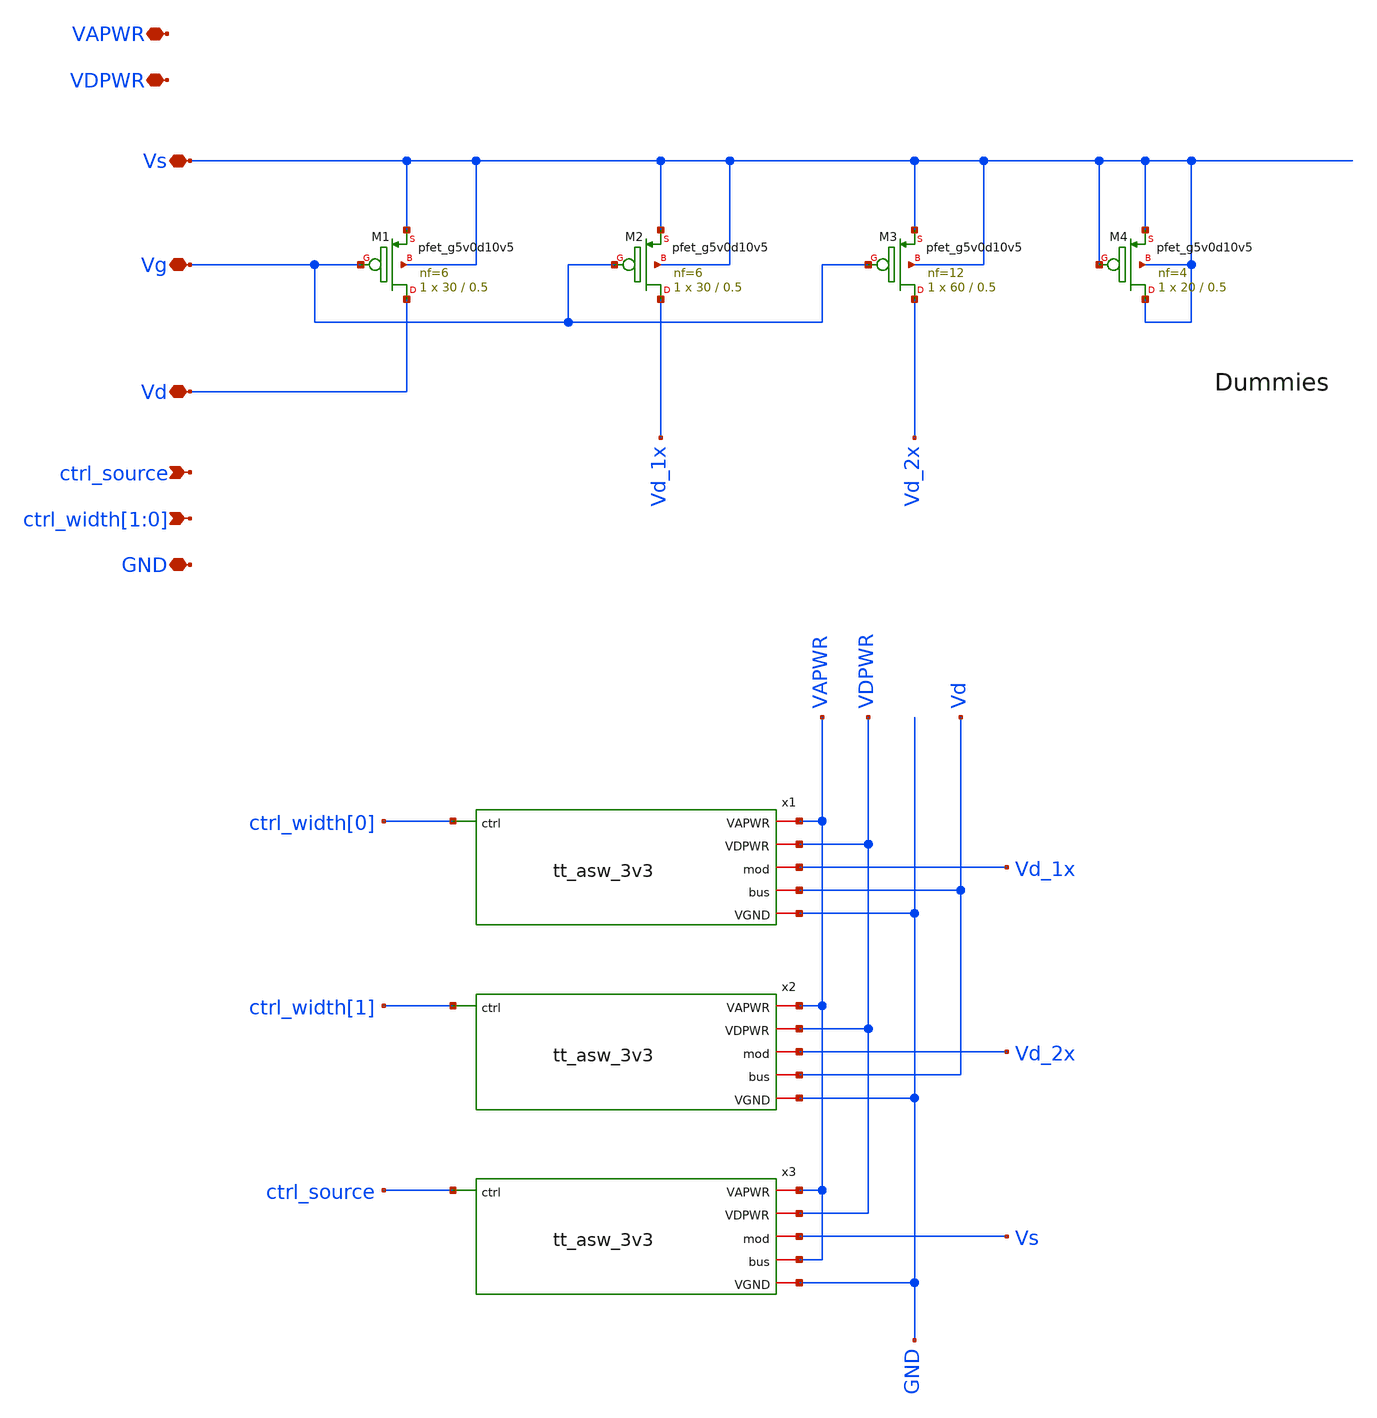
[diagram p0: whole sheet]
** sch_path: tt_um_mosbius/xschem/pmos_prog.sch
**.subckt pmos_prog ctrl_width[1],ctrl_width[0] Vs Vg Vd VAPWR VDPWR GND ctrl_source
*.ipin ctrl_width[1],ctrl_width[0]
*.iopin Vs
*.iopin Vg
*.iopin Vd
*.iopin VAPWR
*.iopin VDPWR
*.iopin GND
*.ipin ctrl_source
x1 GND VDPWR VAPWR ctrl_width[0] Vd_1x Vd tt_asw_3v3
x2 GND VDPWR VAPWR ctrl_width[1] Vd_2x Vd tt_asw_3v3
x3 GND VDPWR VAPWR ctrl_source Vs VAPWR tt_asw_3v3
XM1 Vd Vg Vs Vs sky130_fd_pr__pfet_g5v0d10v5 L=0.5 W=30 nf=6 ad='int((nf+1)/2) * W/nf * 0.29' as='int((nf+2)/2) * W/nf * 0.29'
+ pd='2*int((nf+1)/2) * (W/nf + 0.29)' ps='2*int((nf+2)/2) * (W/nf + 0.29)' nrd='0.29 / W' nrs='0.29 / W'
+ sa=0 sb=0 sd=0 mult=1 m=1
XM2 Vd_1x Vg Vs Vs sky130_fd_pr__pfet_g5v0d10v5 L=0.5 W=30 nf=6 ad='int((nf+1)/2) * W/nf * 0.29' as='int((nf+2)/2) * W/nf * 0.29'
+ pd='2*int((nf+1)/2) * (W/nf + 0.29)' ps='2*int((nf+2)/2) * (W/nf + 0.29)' nrd='0.29 / W' nrs='0.29 / W'
+ sa=0 sb=0 sd=0 mult=1 m=1
XM3 Vd_2x Vg Vs Vs sky130_fd_pr__pfet_g5v0d10v5 L=0.5 W=60 nf=12 ad='int((nf+1)/2) * W/nf * 0.29' as='int((nf+2)/2) * W/nf * 0.29'
+ pd='2*int((nf+1)/2) * (W/nf + 0.29)' ps='2*int((nf+2)/2) * (W/nf + 0.29)' nrd='0.29 / W' nrs='0.29 / W'
+ sa=0 sb=0 sd=0 mult=1 m=1
XM4 Vs Vs Vs Vs sky130_fd_pr__pfet_g5v0d10v5 L=0.5 W=20 nf=4 ad='int((nf+1)/2) * W/nf * 0.29' as='int((nf+2)/2) * W/nf * 0.29'
+ pd='2*int((nf+1)/2) * (W/nf + 0.29)' ps='2*int((nf+2)/2) * (W/nf + 0.29)' nrd='0.29 / W' nrs='0.29 / W'
+ sa=0 sb=0 sd=0 mult=1 m=1
**.ends

* expanding   symbol:  tt_asw_3v3.sym # of pins=6
** sym_path: tt_asw_3v3.sym
** sch_path: tt_asw_3v3.sch
.subckt tt_asw_3v3 VGND VDPWR VAPWR ctrl mod bus
*.iopin mod
*.iopin bus
*.ipin ctrl
*.iopin VGND
*.iopin VDPWR
*.iopin VAPWR
XM1 tgon_n net2 VAPWR VAPWR sky130_fd_pr__pfet_g5v0d10v5 L=0.5 W=0.84 nf=1 ad='int((nf+1)/2) * W/nf * 0.29'
+ as='int((nf+2)/2) * W/nf * 0.29' pd='2*int((nf+1)/2) * (W/nf + 0.29)' ps='2*int((nf+2)/2) * (W/nf + 0.29)'
+ nrd='0.29 / W' nrs='0.29 / W' sa=0 sb=0 sd=0 mult=1 m=1
XM2 tgon_n net2 VGND VGND sky130_fd_pr__nfet_g5v0d10v5 L=0.5 W=0.42 nf=1 ad='int((nf+1)/2) * W/nf * 0.29'
+ as='int((nf+2)/2) * W/nf * 0.29' pd='2*int((nf+1)/2) * (W/nf + 0.29)' ps='2*int((nf+2)/2) * (W/nf + 0.29)'
+ nrd='0.29 / W' nrs='0.29 / W' sa=0 sb=0 sd=0 mult=1 m=1
XM3 tgon net1 VAPWR VAPWR sky130_fd_pr__pfet_g5v0d10v5 L=0.5 W=0.84 nf=1 ad='int((nf+1)/2) * W/nf * 0.29'
+ as='int((nf+2)/2) * W/nf * 0.29' pd='2*int((nf+1)/2) * (W/nf + 0.29)' ps='2*int((nf+2)/2) * (W/nf + 0.29)'
+ nrd='0.29 / W' nrs='0.29 / W' sa=0 sb=0 sd=0 mult=1 m=1
XM4 tgon net1 VGND VGND sky130_fd_pr__nfet_g5v0d10v5 L=0.5 W=0.42 nf=1 ad='int((nf+1)/2) * W/nf * 0.29'
+ as='int((nf+2)/2) * W/nf * 0.29' pd='2*int((nf+1)/2) * (W/nf + 0.29)' ps='2*int((nf+2)/2) * (W/nf + 0.29)'
+ nrd='0.29 / W' nrs='0.29 / W' sa=0 sb=0 sd=0 mult=1 m=1
XM5 bus tgon_n mod VAPWR sky130_fd_pr__pfet_g5v0d10v5 L=0.5 W=180 nf=18 ad='int((nf+1)/2) * W/nf * 0.29'
+ as='int((nf+2)/2) * W/nf * 0.29' pd='2*int((nf+1)/2) * (W/nf + 0.29)' ps='2*int((nf+2)/2) * (W/nf + 0.29)'
+ nrd='0.29 / W' nrs='0.29 / W' sa=0 sb=0 sd=0 mult=1 m=1
XM6 bus tgon mod VGND sky130_fd_pr__nfet_g5v0d10v5 L=0.5 W=60 nf=12 ad='int((nf+1)/2) * W/nf * 0.29'
+ as='int((nf+2)/2) * W/nf * 0.29' pd='2*int((nf+1)/2) * (W/nf + 0.29)' ps='2*int((nf+2)/2) * (W/nf + 0.29)'
+ nrd='0.29 / W' nrs='0.29 / W' sa=0 sb=0 sd=0 mult=1 m=1
XM7 ctrl_n ctrl VGND VGND sky130_fd_pr__nfet_01v8 L=0.15 W=0.42 nf=1 ad='int((nf+1)/2) * W/nf * 0.29'
+ as='int((nf+2)/2) * W/nf * 0.29' pd='2*int((nf+1)/2) * (W/nf + 0.29)' ps='2*int((nf+2)/2) * (W/nf + 0.29)'
+ nrd='0.29 / W' nrs='0.29 / W' sa=0 sb=0 sd=0 mult=1 m=1
XM8 ctrl_n ctrl VDPWR VDPWR sky130_fd_pr__pfet_01v8_hvt L=0.15 W=1 nf=1 ad='int((nf+1)/2) * W/nf * 0.29'
+ as='int((nf+2)/2) * W/nf * 0.29' pd='2*int((nf+1)/2) * (W/nf + 0.29)' ps='2*int((nf+2)/2) * (W/nf + 0.29)'
+ nrd='0.29 / W' nrs='0.29 / W' sa=0 sb=0 sd=0 mult=1 m=1
XM9 net1 ctrl VGND VGND sky130_fd_pr__nfet_g5v0d10v5 L=0.5 W=0.42 nf=1 ad='int((nf+1)/2) * W/nf * 0.29'
+ as='int((nf+2)/2) * W/nf * 0.29' pd='2*int((nf+1)/2) * (W/nf + 0.29)' ps='2*int((nf+2)/2) * (W/nf + 0.29)'
+ nrd='0.29 / W' nrs='0.29 / W' sa=0 sb=0 sd=0 mult=1 m=1
XM10 net2 ctrl_n VGND VGND sky130_fd_pr__nfet_g5v0d10v5 L=0.5 W=0.42 nf=1 ad='int((nf+1)/2) * W/nf * 0.29'
+ as='int((nf+2)/2) * W/nf * 0.29' pd='2*int((nf+1)/2) * (W/nf + 0.29)' ps='2*int((nf+2)/2) * (W/nf + 0.29)'
+ nrd='0.29 / W' nrs='0.29 / W' sa=0 sb=0 sd=0 mult=1 m=1
XM11 net1 net2 net3 VAPWR sky130_fd_pr__pfet_g5v0d10v5 L=0.5 W=0.42 nf=1 ad='int((nf+1)/2) * W/nf * 0.29'
+ as='int((nf+2)/2) * W/nf * 0.29' pd='2*int((nf+1)/2) * (W/nf + 0.29)' ps='2*int((nf+2)/2) * (W/nf + 0.29)'
+ nrd='0.29 / W' nrs='0.29 / W' sa=0 sb=0 sd=0 mult=1 m=1
XM12 net2 net1 net4 VAPWR sky130_fd_pr__pfet_g5v0d10v5 L=0.5 W=0.42 nf=1 ad='int((nf+1)/2) * W/nf * 0.29'
+ as='int((nf+2)/2) * W/nf * 0.29' pd='2*int((nf+1)/2) * (W/nf + 0.29)' ps='2*int((nf+2)/2) * (W/nf + 0.29)'
+ nrd='0.29 / W' nrs='0.29 / W' sa=0 sb=0 sd=0 mult=1 m=1
XM13 net3 net1 VAPWR VAPWR sky130_fd_pr__pfet_g5v0d10v5 L=0.5 W=0.42 nf=1 ad='int((nf+1)/2) * W/nf * 0.29'
+ as='int((nf+2)/2) * W/nf * 0.29' pd='2*int((nf+1)/2) * (W/nf + 0.29)' ps='2*int((nf+2)/2) * (W/nf + 0.29)'
+ nrd='0.29 / W' nrs='0.29 / W' sa=0 sb=0 sd=0 mult=1 m=1
XM14 net4 net2 VAPWR VAPWR sky130_fd_pr__pfet_g5v0d10v5 L=0.5 W=0.42 nf=1 ad='int((nf+1)/2) * W/nf * 0.29'
+ as='int((nf+2)/2) * W/nf * 0.29' pd='2*int((nf+1)/2) * (W/nf + 0.29)' ps='2*int((nf+2)/2) * (W/nf + 0.29)'
+ nrd='0.29 / W' nrs='0.29 / W' sa=0 sb=0 sd=0 mult=1 m=1
.ends

.end
